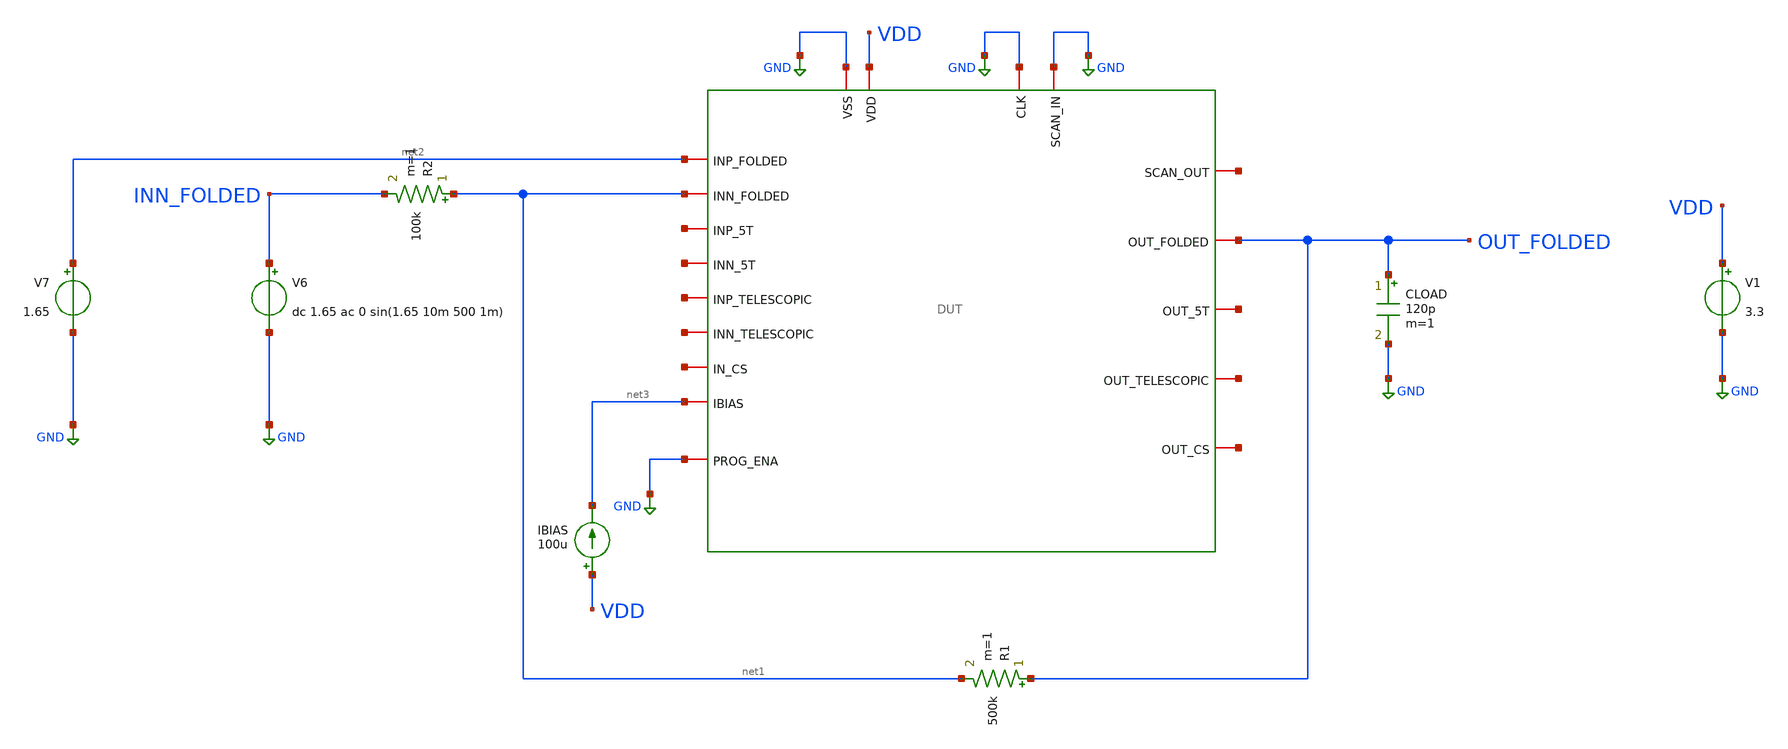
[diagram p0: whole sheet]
** sch_path: designs/libs/verification/start_up_cir/folded/default_inverting_folded.sch
**.subckt default_inverting_folded
V1 VDD GND 3.3
CLOAD OUT_FOLDED GND 120p m=1
R1 OUT_FOLDED net1 500k m=1
R2 net1 INN_FOLDED 100k m=1
V6 INN_FOLDED GND dc 1.65 ac 0 sin(1.65 10m 500 1m)
V7 net2 GND 1.65
IBIAS VDD net3 100u
x1 GND net4 GND GND VDD OUT_FOLDED net2 net5 net3 net1 net6 net7 net8 net9 net10 net11 net12 GND DUT
**** begin user architecture code

.include $::180MCU_MODELS/design.ngspice
.lib $::180MCU_MODELS/sm141064.ngspice typical




.include /foss/designs/libs/pex/DUT.spice
.control
tran 1u 5m

plot v(out_folded) v(inn_folded)
wrdata /foss/designs/libs/verification/start_up_cir/folded/default.csv v(out_folded) v(inn_folded)

meas tran vout_pp pp v(out_folded) from=2m to=5m
meas tran vin_pp pp v(inn_folded) from=2m to=5m
let gain = vout_pp / vin_pp
print gain

meas tran vout_dc avg v(out_folded) from=2m to=5m
meas tran vin_dc avg v(inn_folded) from=2m to=5m
let dc_offset = vout_dc - vin_dc
let input_offset = dc_offset / 6
print vout_dc vin_dc dc_offset input_offset

let ideal_gain = 5
let gain_error_pct = (ideal_gain - gain) / ideal_gain * 100
print gain_error_pct

meas tran idd avg i(v1) from=2m to=5m
let power = abs(idd) * 3.3
print idd power
.endc


**** end user architecture code
**.ends
.GLOBAL GND
.end
